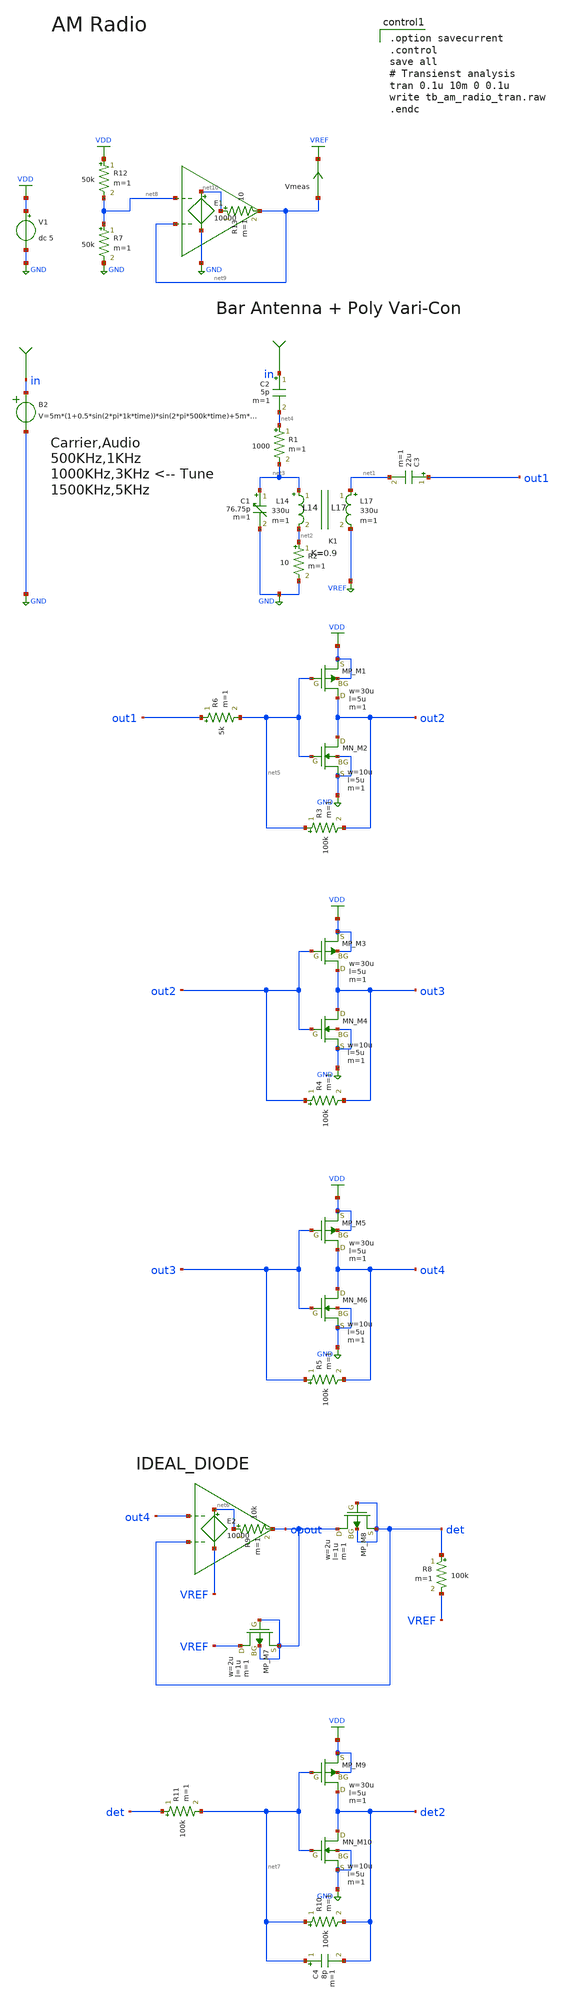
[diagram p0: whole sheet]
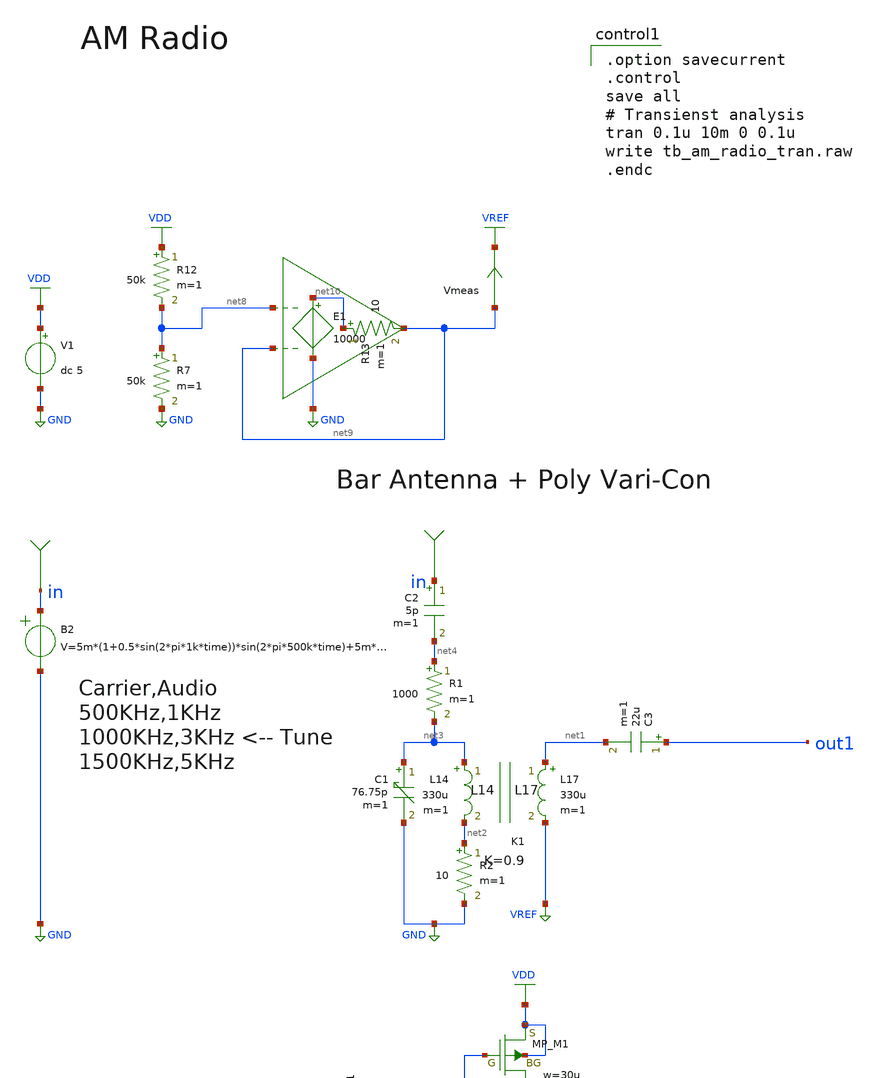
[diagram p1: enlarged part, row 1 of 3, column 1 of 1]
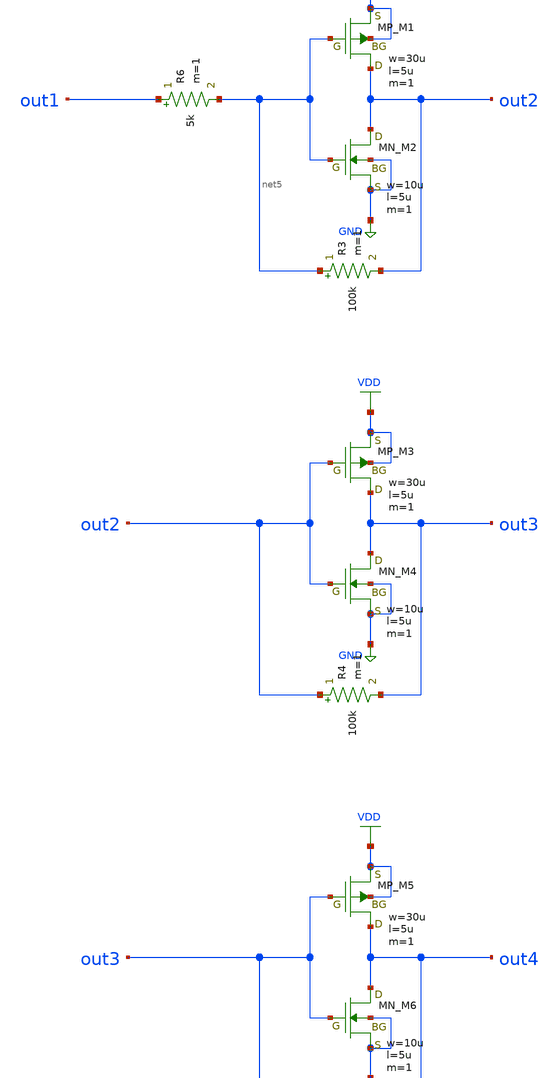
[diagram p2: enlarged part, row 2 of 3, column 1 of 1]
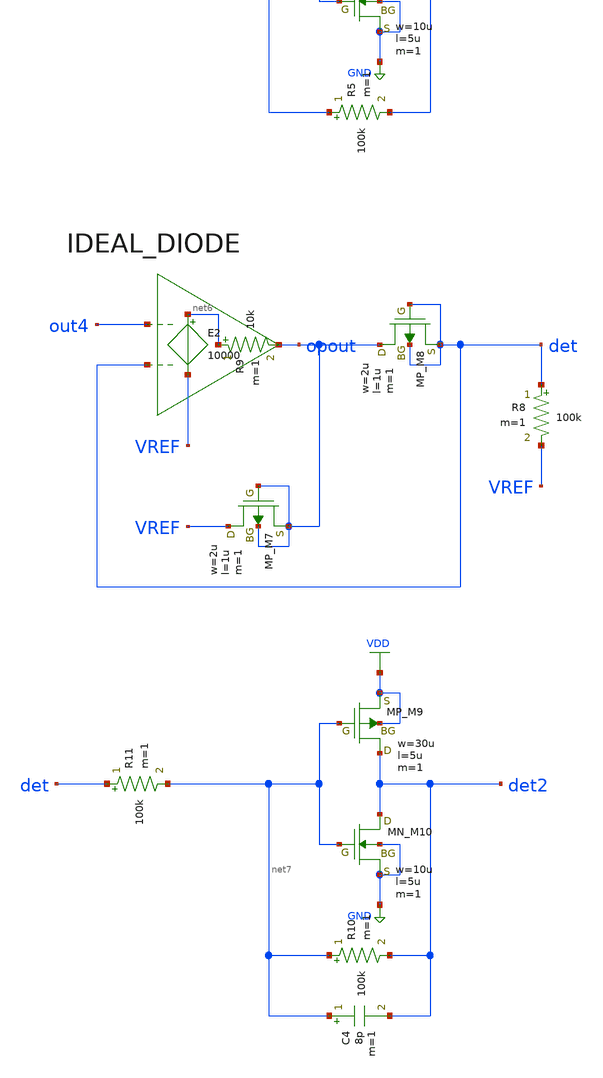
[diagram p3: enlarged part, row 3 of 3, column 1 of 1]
** sch_path: member_project/AM_Radio/Yamada3/xschem/tb_am_radio.sch
**.subckt tb_am_radio
V1 VDD GND dc 5
B2 in GND
+ V=5m*(1+0.5*sin(2*pi*1k*time))*sin(2*pi*500k*time)+5m*(1+0.5*sin(2*pi*3k*time))*sin(2*pi*1000k*time)+5m*(1+0.5*sin(2*pi*5k*time))*sin(2*pi*1500k*time)
C1 net3 GND 76.75p m=1
L14 net3 net2 330u m=1
K1 L17 L14 0.9
L17 net1 VREF 330u m=1
R2 net2 GND 10 m=1
R1 net4 net3 1000 m=1
C2 in net4 5p m=1
XM1 out2 net5 VDD VDD PMOS w=30u l=5u as=0 ad=0 ps=0 pd=0 nrd=0 nrs=0 m=1
XM2 out2 net5 GND GND NMOS w=10u l=5u as=0 ad=0 ps=0 pd=0 nrd=0 nrs=0 m=1
R3 net5 out2 100k m=1
C3 out1 net1 22u m=1
XM3 out3 out2 VDD VDD PMOS w=30u l=5u as=0 ad=0 ps=0 pd=0 nrd=0 nrs=0 m=1
XM4 out3 out2 GND GND NMOS w=10u l=5u as=0 ad=0 ps=0 pd=0 nrd=0 nrs=0 m=1
R4 out2 out3 100k m=1
XM5 out4 out3 VDD VDD PMOS w=30u l=5u as=0 ad=0 ps=0 pd=0 nrd=0 nrs=0 m=1
XM6 out4 out3 GND GND NMOS w=10u l=5u as=0 ad=0 ps=0 pd=0 nrd=0 nrs=0 m=1
R5 out3 out4 100k m=1
R6 out1 net5 5k m=1
E2 net6 VREF out4 det 10000
XM7 VREF opout opout opout PMOS w=2u l=1u as=0 ad=0 ps=0 pd=0 nrd=0 nrs=0 m=1
XM8 opout det det det PMOS w=2u l=1u as=0 ad=0 ps=0 pd=0 nrd=0 nrs=0 m=1
R8 det VREF 100k m=1
R9 net6 opout 10k m=1
XM9 det2 net7 VDD VDD PMOS w=30u l=5u as=0 ad=0 ps=0 pd=0 nrd=0 nrs=0 m=1
XM10 det2 net7 GND GND NMOS w=10u l=5u as=0 ad=0 ps=0 pd=0 nrd=0 nrs=0 m=1
R10 net7 det2 100k m=1
R11 det net7 100k m=1
C4 net7 det2 8p m=1
Vmeas net9 VREF 0
.save i(vmeas)
R7 net8 GND 50k m=1
R12 VDD net8 50k m=1
E1 net10 GND net8 net9 10000
R13 net10 net9 10 m=1
**** begin user architecture code

.option savecurrent
.control
save all
# Transienst analysis
tran 0.1u 10m 0 0.1u
write tb_am_radio_tran.raw
.endc

 .include $::LIB/ip62_models
**** end user architecture code
**.ends
.GLOBAL GND
.GLOBAL VDD
.GLOBAL VREF
.end
